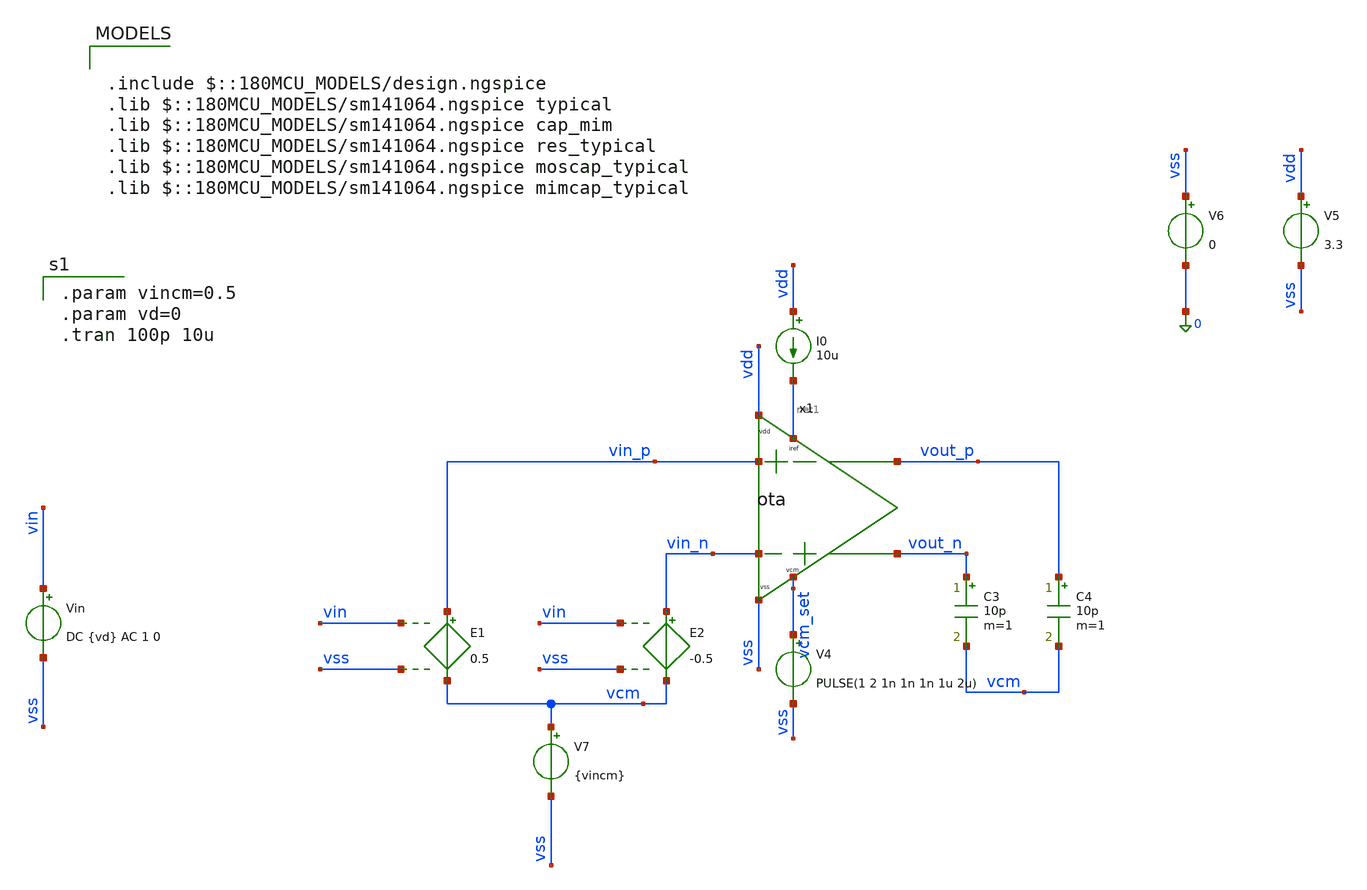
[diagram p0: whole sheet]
** sch_path: xschem/archive/ota/ota_cmfb_transient.sch
**.subckt ota_cmfb_transient
x1 vdd net1 vin_p vin_n vss vcm_set vout_n vout_p ota
I0 vdd net1 10u
V4 vcm_set vss PULSE(1 2 1n 1n 1n 1u 2u)
C3 vout_n vcm 10p m=1
C4 vout_p vcm 10p m=1
V5 vdd vss 3.3
V6 vss 0 0
V7 vcm vss {vincm}
E1 vin_p vcm vin vss 0.5
E2 vin_n vcm vin vss -0.5
Vin vin vss DC {vd} AC 1 0
**** begin user architecture code

.include $::180MCU_MODELS/design.ngspice
.lib $::180MCU_MODELS/sm141064.ngspice typical
.lib $::180MCU_MODELS/sm141064.ngspice cap_mim
.lib $::180MCU_MODELS/sm141064.ngspice res_typical
.lib $::180MCU_MODELS/sm141064.ngspice moscap_typical
.lib $::180MCU_MODELS/sm141064.ngspice mimcap_typical


.param vincm=0.5
.param vd=0
.tran 100p 10u

**** end user architecture code
**.ends
.end
